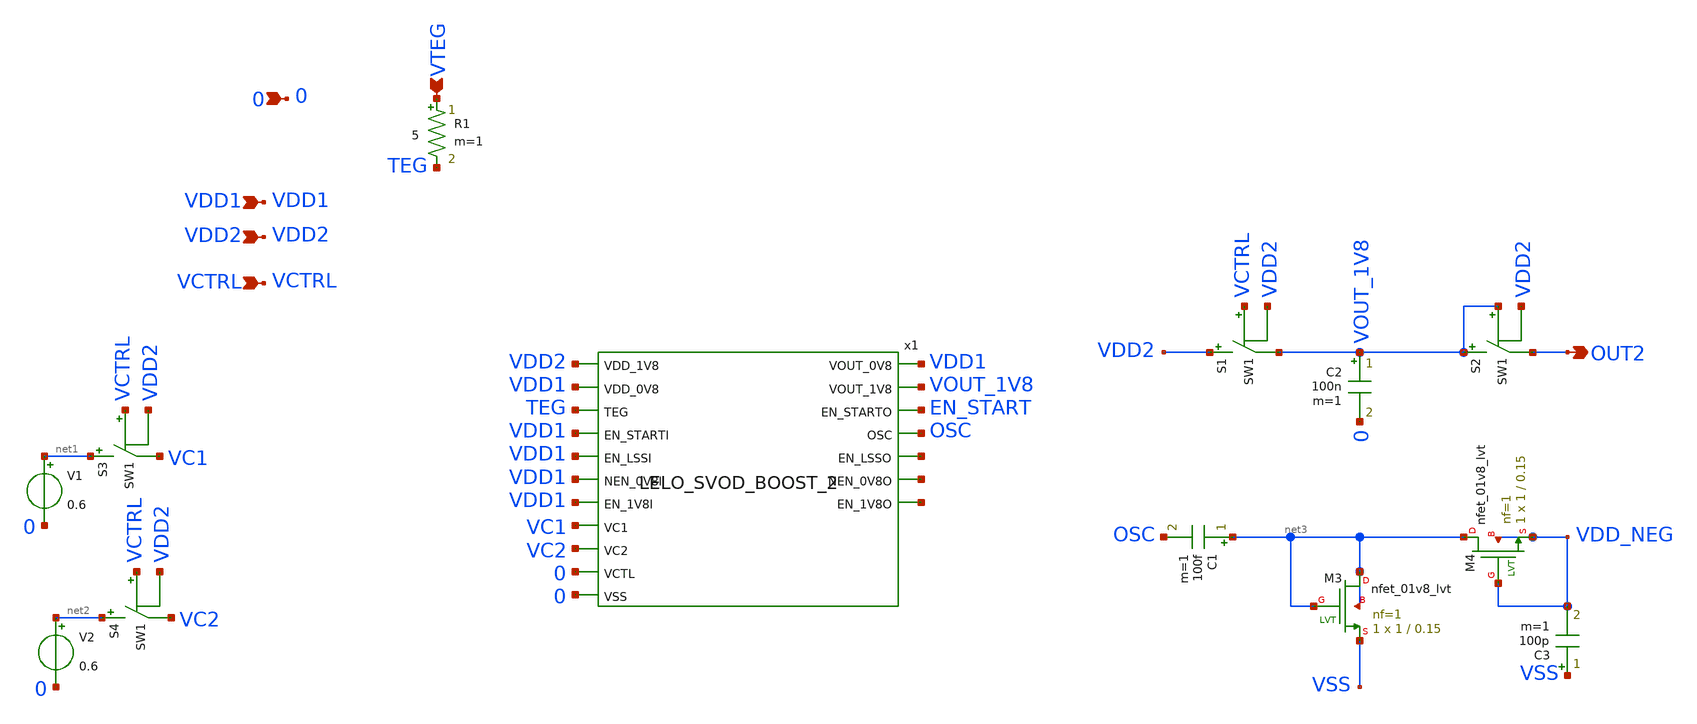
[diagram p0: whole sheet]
** sch_path: design/LELO_SVOD_SKY130A/LELO_SVOD_1V8_BOOST.sch
**.subckt LELO_SVOD_1V8_BOOST VTEG 0 OUT2 VDD1 VDD2 VCTRL
*.ipin VTEG
*.ipin 0
*.opin OUT2
*.ipin VDD1
*.ipin VDD2
*.ipin VCTRL
R1 VTEG TEG 5 m=1
S2 VOUT_1V8 OUT2 VOUT_1V8 VDD2 SW1
x1 VDD1 VDD2 VDD1 TEG VDD1 VDD1 VDD1 VDD1 VOUT_1V8 VC1 VC2 0 0 EN_START OSC net4 net5 net6
+ LELO_SVOD_BOOST_2
C2 VOUT_1V8 0 100n m=1
V1 net1 0 0.6
V2 net2 0 0.6
S1 VDD2 VOUT_1V8 VCTRL VDD2 SW1
S3 net1 VC1 VCTRL VDD2 SW1
S4 net2 VC2 VCTRL VDD2 SW1
C1 net3 OSC 100f m=1
XM3 net3 net3 VSS net3 sky130_fd_pr__nfet_01v8_lvt L=0.15 W=1 nf=1 ad='int((1 + 1)/2) * 1 / 1 * 0.29'
+ as='int((1 + 2)/2) * 1 / 1 * 0.29' pd='2*int((1 + 1)/2) * (1 / 1 + 0.29)' ps='2*int((1 + 2)/2) * (1 / 1 + 0.29)'
+ nrd='0.29 / 1 ' nrs='0.29 / 1 ' sa=0 sb=0 sd=0 mult=1 m=1
XM4 net3 VDD_NEG VDD_NEG VDD_NEG sky130_fd_pr__nfet_01v8_lvt L=0.15 W=1 nf=1 ad='int((1 + 1)/2) * 1 / 1 * 0.29'
+ as='int((1 + 2)/2) * 1 / 1 * 0.29' pd='2*int((1 + 1)/2) * (1 / 1 + 0.29)' ps='2*int((1 + 2)/2) * (1 / 1 + 0.29)'
+ nrd='0.29 / 1 ' nrs='0.29 / 1 ' sa=0 sb=0 sd=0 mult=1 m=1
C3 VSS VDD_NEG 100p m=1
**.ends
**** begin user architecture code
.MODEL SW1 SW   VT=0 VH=0.001  RON=0.001 ROFF=10G
**** end user architecture code
.end
